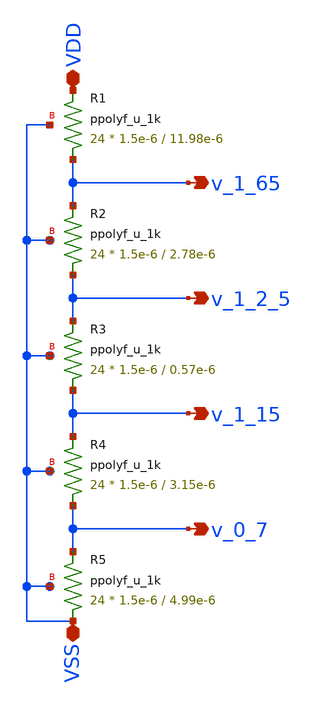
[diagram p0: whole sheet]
** sch_path: schematics/voltage_reference.sch
**.subckt voltage_reference VDD VSS v_1_65 v_1_2_5 v_1_15 v_0_7
*.iopin VDD
*.iopin VSS
*.opin v_1_65
*.opin v_1_2_5
*.opin v_1_15
*.opin v_0_7
XR1 v_1_65 VDD VSS ppolyf_u_1k r_width=1.5e-6 r_length=11.98e-6 m=24
XR2 v_1_2_5 v_1_65 VSS ppolyf_u_1k r_width=1.5e-6 r_length=2.78e-6 m=24
XR3 v_1_15 v_1_2_5 VSS ppolyf_u_1k r_width=1.5e-6 r_length=0.57e-6 m=24
XR4 v_0_7 v_1_15 VSS ppolyf_u_1k r_width=1.5e-6 r_length=3.15e-6 m=24
XR5 VSS v_0_7 VSS ppolyf_u_1k r_width=1.5e-6 r_length=4.99e-6 m=24
**.ends
.end
